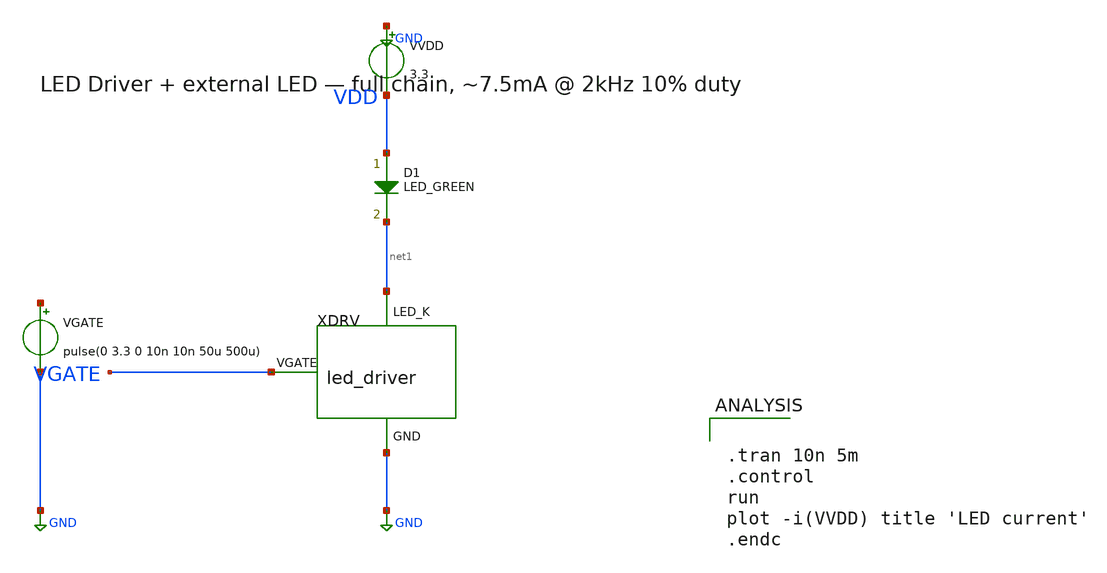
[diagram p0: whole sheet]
** sch_path: ps-led-driver/schematic/led_driver_with_led.sch
**.subckt led_driver_with_led
VVDD GND VDD 3.3
D1 VDD net1 LED_GREEN area=1e-6
XDRV VGATE net1 GND led_driver
VGATE net2 GND pulse(0 3.3 0 10n 10n 50u 500u)
**** begin user architecture code


.include /foss/pdks/gf180mcuD/libs.tech/ngspice/design.ngspice
.lib /foss/pdks/gf180mcuD/libs.tech/ngspice/sm141064.ngspice typical
.model LED_GREEN D(Is=1e-16 N=2.0 Rs=5 Vj=1.8 Cjo=10p)




.tran 10n 5m
.control
run
plot -i(VVDD) title 'LED current'
.endc


**** end user architecture code
**.ends

* expanding   symbol:  led_driver.sym # of pins=3
** sym_path: ps-led-driver/schematic/led_driver.sym
** sch_path: ps-led-driver/schematic/led_driver.sch
.subckt led_driver VGATE LED_K GND
*.ipin VGATE
*.iopin LED_K
*.iopin GND
R_set LED_K net1 270 m=1
XXM1 net1 VGATE GND GND nfet_03v3 L=0.5u W=20u nf=1 ad='int((nf+1)/2) * W/nf * 0.18u' as='int((nf+2)/2) * W/nf * 0.18u'
+ pd='2*int((nf+1)/2) * (W/nf + 0.18u)' ps='2*int((nf+2)/2) * (W/nf + 0.18u)' nrd='0.18u / W' nrs='0.18u / W'
+ sa=0 sb=0 sd=0 m=1
.ends

.GLOBAL GND
.end
